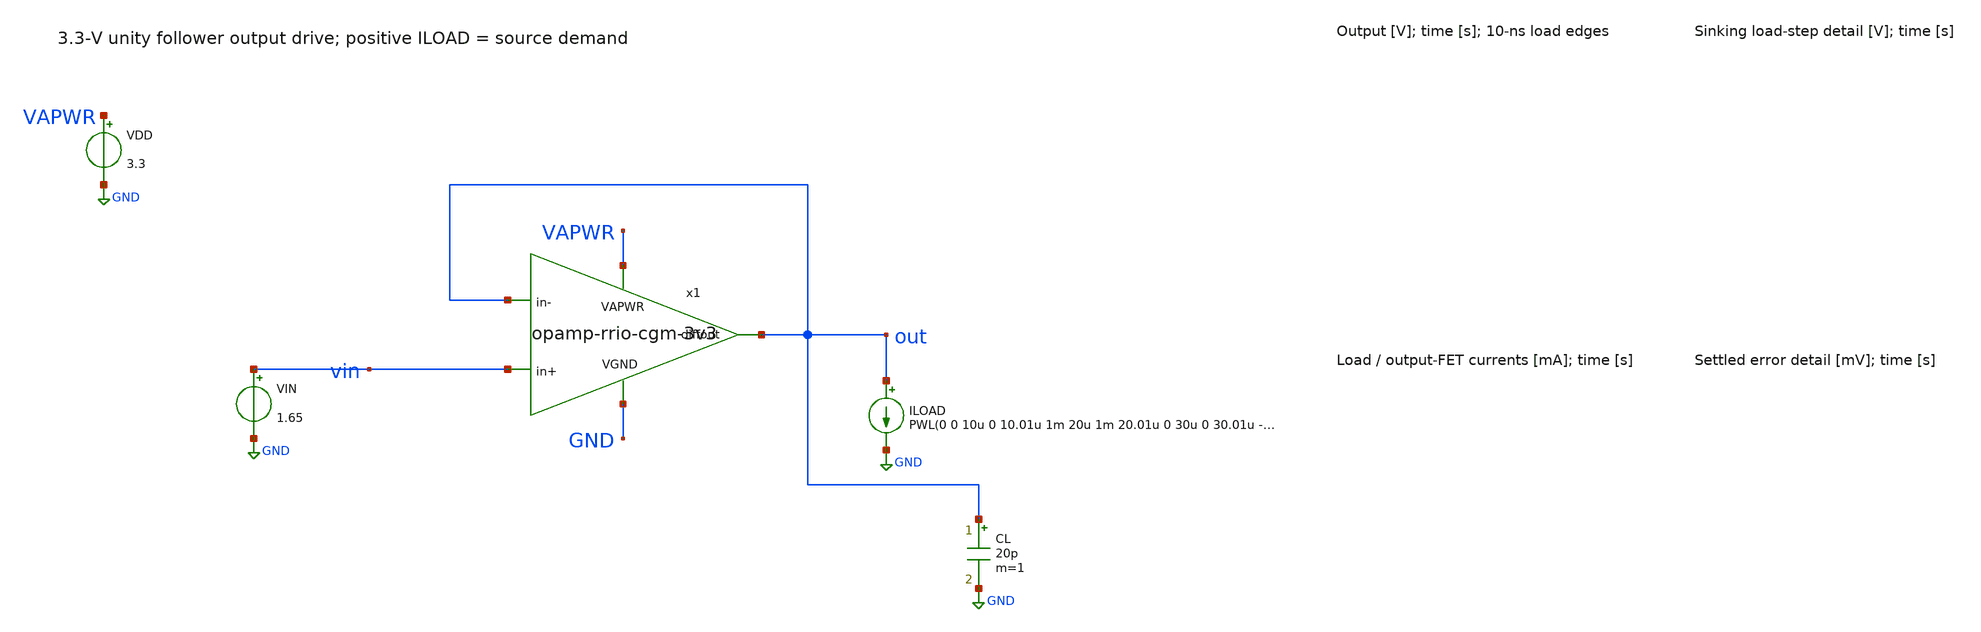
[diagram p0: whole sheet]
** sch_path: xschem/testbench_output_tran_3v3.sch
**.subckt testbench_output_tran_3v3
x1 VAPWR out vin out GND opamp-rrio-cgm-3v3
VDD VAPWR GND 3.3
VIN vin GND 1.65
ILOAD out GND PWL(0 0 10u 0 10.01u 1m 20u 1m 20.01u 0 30u 0 30.01u -1m 40u -1m 40.01u 0 50u 0)
CL out GND 20p m=1
**** begin user architecture code
 .lib $::SKYWATER_MODELS/sky130.lib.spice tt

.options klu itl1=100 reltol=.0001
.nodeset v(x1.net1)=2.55229105
.nodeset v(x1.net3)=0.866789395
.nodeset v(x1.net4)=0.29731059
.nodeset v(x1.net5)=0.297227056
.nodeset v(x1.net7)=2.03109432
.nodeset v(x1.net9)=1.08535928
.nodeset v(x1.fc_pref)=2.02894826
.nodeset v(x1.fc_nref)=1.08255405
.nodeset v(x1.bias1)=2.05405688
.nodeset v(x1.bias2)=2.04452255
.nodeset v(x1.bias3)=1.14047666
.nodeset v(x1.bias4)=1.04710014
.nodeset v(x1.bias)=1.65
.nodeset v(out)=1.65 v(x1.xb.xref.vbiasn)=.91 v(x1.xb.xref.vbiasp)=2.05 v(x1.xb.xref.vstartup)=.1
.control
set wr_singlescale
set wr_vecnames
save all @iload[current] @m.x1.xm29.msky130_fd_pr__pfet_g5v0d10v5[id]
+ @m.x1.xm32.msky130_fd_pr__nfet_g5v0d10v5[id] @m.x1.xb.xref.xm1.msky130_fd_pr__pfet_g5v0d10v5[id]
tran 5n 50u 0 5n

* Reject roots outside the SKY130 HV gate-voltage range.
let physical_bias_peak = vecmax(abs(v(x1.bias)))
if physical_bias_peak > 5.5
echo PHYSICAL_BIAS_ERROR: invalid PDK operating point
quit 1
end
let error_mV=1000*(v(out)-v(vin))
let load_mA=1000*@iload[current]
let source_mA=1000*@m.x1.xm29.msky130_fd_pr__pfet_g5v0d10v5[id]
let sink_mA=1000*@m.x1.xm32.msky130_fd_pr__nfet_g5v0d10v5[id]
write testbench_output_tran_3v3.raw all
wrdata testbench_output_tran_3v3.dat v(vin) v(out) @iload[current] i(VDD)
+ @m.x1.xm29.msky130_fd_pr__pfet_g5v0d10v5[id] @m.x1.xm32.msky130_fd_pr__nfet_g5v0d10v5[id] @m.x1.xb.xref.xm1.msky130_fd_pr__pfet_g5v0d10v5[id]
.endc

**** end user architecture code
**.ends
.GLOBAL GND
.end
